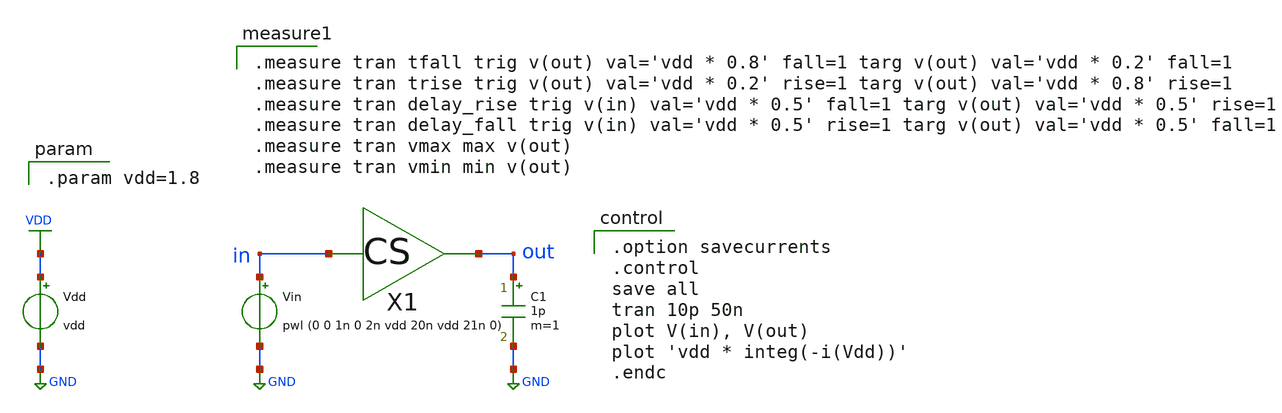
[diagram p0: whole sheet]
** sch_path: xschem/tb/tran_02_measure.sch
**.subckt tran_02_measure
Vdd VDD GND vdd
Vin in GND pwl (0 0 1n 0 2n vdd 20n vdd 21n 0)
X1 in out cs
C1 out GND 1p m=1
**** begin user architecture code

.model nch nmos ( version=4.7 level=54 lmin=0.1u lmax=20u wmin=0.1u wmax=10u  )
.model pch pmos ( version=4.7 level=54 lmin=0.1u lmax=20u wmin=0.1u wmax=10u  )


.option savecurrents
.control
save all
tran 10p 50n
plot V(in), V(out)
plot 'vdd * integ(-i(Vdd))'
.endc


.param vdd=1.8


.measure tran tfall trig v(out) val='vdd * 0.8' fall=1 targ v(out) val='vdd * 0.2' fall=1
.measure tran trise trig v(out) val='vdd * 0.2' rise=1 targ v(out) val='vdd * 0.8' rise=1
.measure tran delay_rise trig v(in) val='vdd * 0.5' fall=1 targ v(out) val='vdd * 0.5' rise=1
.measure tran delay_fall trig v(in) val='vdd * 0.5' rise=1 targ v(out) val='vdd * 0.5' fall=1
.measure tran vmax max v(out)
.measure tran vmin min v(out)

**** end user architecture code
**.ends

* expanding   symbol:  cs.sym # of pins=2
** sym_path: xschem/tb/cs.sym
** sch_path: xschem/tb/cs.sch
.subckt cs in out
*.ipin in
*.opin out
R1 VDD out 1k m=1
M1 out in GND GND nch w=3.6u l=0.18u m=1
.ends

.GLOBAL VDD
.GLOBAL GND
.end
